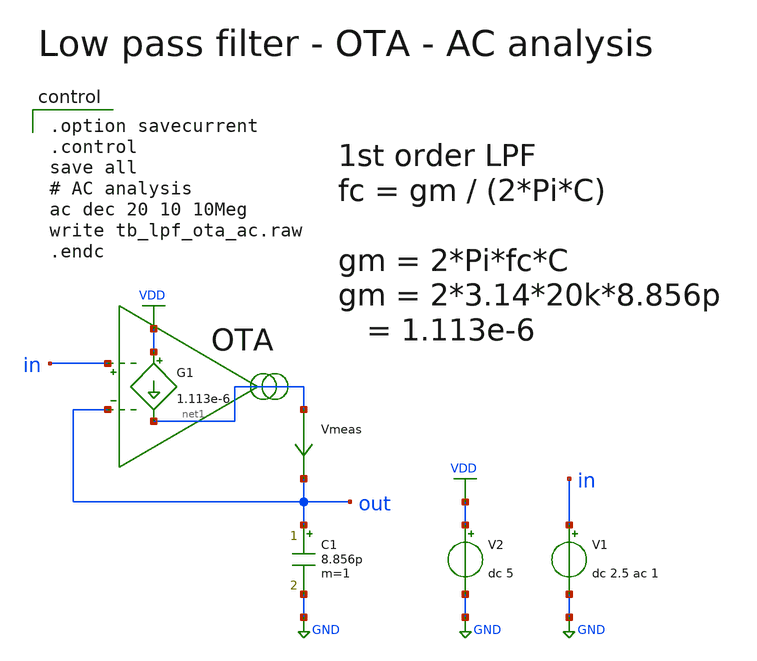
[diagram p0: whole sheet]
** sch_path: member_project/AM_Radio/Yamada3/xschem/tb_lpf_ota_ac.sch
**.subckt tb_lpf_ota_ac
V2 VDD GND dc 5
V1 in GND dc 2.5 ac 1
G1 VDD net1 in out 1.113e-6
Vmeas net1 out 0
.save i(vmeas)
C1 out GND 8.856p m=1
**** begin user architecture code

.option savecurrent
.control
save all
# AC analysis
ac dec 20 10 10Meg
write tb_lpf_ota_ac.raw
.endc

**** end user architecture code
**.ends
.GLOBAL GND
.GLOBAL VDD
.end
